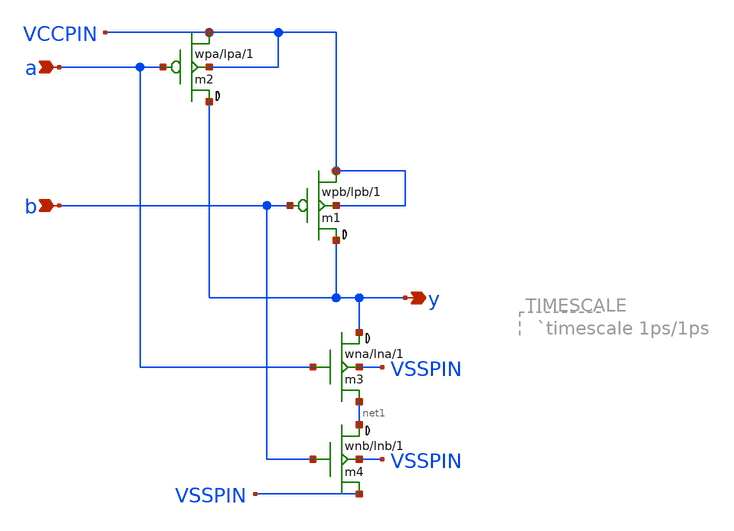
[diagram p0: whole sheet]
** sch_path: xschem_libraries_oa/rom8k/lvnand2/schematic/lvnand2.sch
* Copyright (C) 1998-2024 Stefan Frederik Schippers
* This program is free software; you can redistribute it and/or modify
* it under the terms of the GNU General Public License as published by
* the Free Software Foundation; either version 2 of the License, or
* (at your option) any later version.
* This program is distributed in the hope that it will be useful,
* but WITHOUT ANY WARRANTY; without even the implied warranty of
* MERCHANTABILITY or FITNESS FOR A PARTICULAR PURPOSE.  See the
* GNU General Public License for more details.
* You should have received a copy of the GNU General Public License
* along with this program; if not, write to the Free Software
**.subckt lvnand2 y a b
*.opin y
*.ipin a
*.ipin b
m2 y a VCCPIN VCCPIN cmosp w=wpa l=lpa ad='wpa *4.6u' as='wpa *4.6u' pd='wpa *2+9.2u' ps='wpa *2+9.2u'
+ m=1
m1 y b VCCPIN VCCPIN cmosp w=wpb l=lpb ad='wpb *4.6u' as='wpb *4.6u' pd='wpb *2+9.2u' ps='wpb *2+9.2u'
+ m=1
m3 y a net1 VSSPIN cmosn w=wna l=lna ad='wna *4.3u' as='wna *4.3u' pd='wna *2+8.6u' ps='wna *2+8.6u'
+ m=1
m4 net1 b VSSPIN VSSPIN cmosn w=wnb l=lnb ad='wnb *4.3u' as='wnb *4.3u' pd='wnb *2+8.6u' ps='wnb *2+8.6u'
+ m=1
**.ends
.end
